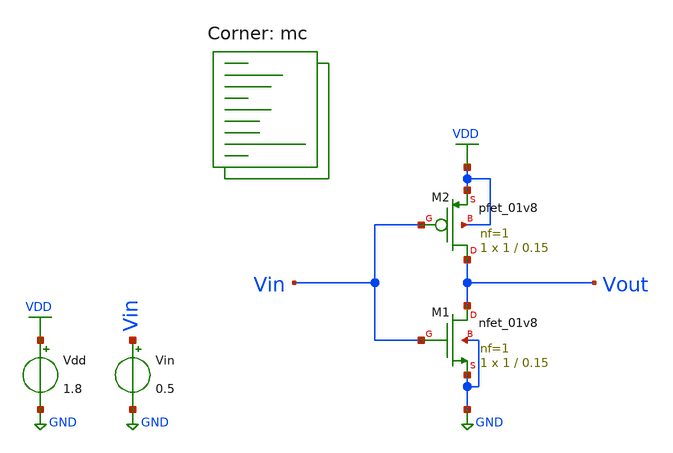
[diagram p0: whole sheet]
** sch_path: projects/montecarlo/xschem_ngspice/inverter/inverter_monte_carlo.sch
**.subckt inverter_monte_carlo
XM1 Vout Vin GND GND sky130_fd_pr__nfet_01v8 L=0.15 W=1 nf=1 ad='int((nf+1)/2) * W/nf * 0.29' as='int((nf+2)/2) * W/nf * 0.29'
+ pd='2*int((nf+1)/2) * (W/nf + 0.29)' ps='2*int((nf+2)/2) * (W/nf + 0.29)' nrd='0.29 / W' nrs='0.29 / W'
+ sa=0 sb=0 sd=0 mult=1 m=1
XM2 Vout Vin VDD VDD sky130_fd_pr__pfet_01v8 L=0.15 W=1 nf=1 ad='int((nf+1)/2) * W/nf * 0.29' as='int((nf+2)/2) * W/nf * 0.29'
+ pd='2*int((nf+1)/2) * (W/nf + 0.29)' ps='2*int((nf+2)/2) * (W/nf + 0.29)' nrd='0.29 / W' nrs='0.29 / W'
+ sa=0 sb=0 sd=0 mult=1 m=1
Vdd VDD GND 1.8
Vin Vin GND 0.5
**** begin user architecture code



.option wnflag=1

.control

  let runs=10
  let run=1

  dowhile run <= runs
    save all
    dc vin 0 1.8 0.01
    write inverter_monte_carlo_mc.raw
    set appendwrite
    reset
    let run = run + 1
  end

.endc



.lib $::SKYWATER_MODELS/sky130.lib.spice mc
**** end user architecture code
**.ends
.GLOBAL VDD
.GLOBAL GND
.end
